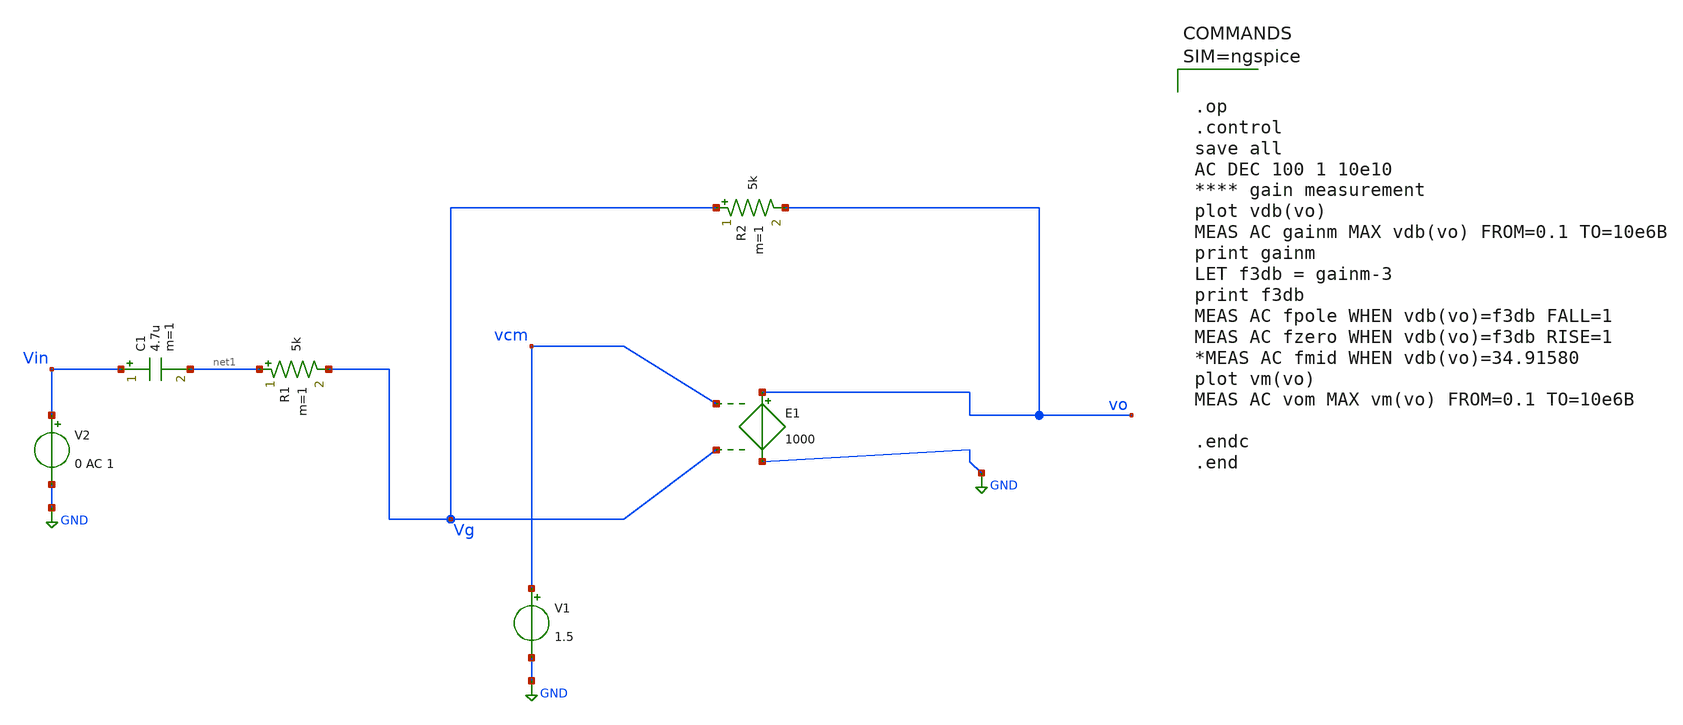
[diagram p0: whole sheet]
** sch_path: Work/xschem/op_sym_sim.sch
**.subckt op_sym_sim
R1 net1 Vg 5k m=1
C1 Vin net1 4.7u m=1
V1 vcm GND 1.5
V2 Vin GND 0 AC 1
R2 Vg vo 5k m=1
E1 vo GND vcm Vg 1000
**** begin user architecture code



.op
.control
save all
AC DEC 100 1 10e10
**** gain measurement
plot vdb(vo)
MEAS AC gainm MAX vdb(vo) FROM=0.1 TO=10e6B
print gainm
LET f3db = gainm-3
print f3db
MEAS AC fpole WHEN vdb(vo)=f3db FALL=1
MEAS AC fzero WHEN vdb(vo)=f3db RISE=1
*MEAS AC fmid WHEN vdb(vo)=34.91580
plot vm(vo)
MEAS AC vom MAX vm(vo) FROM=0.1 TO=10e6B

.endc
.end





**** end user architecture code
**.ends
.GLOBAL GND
.end
